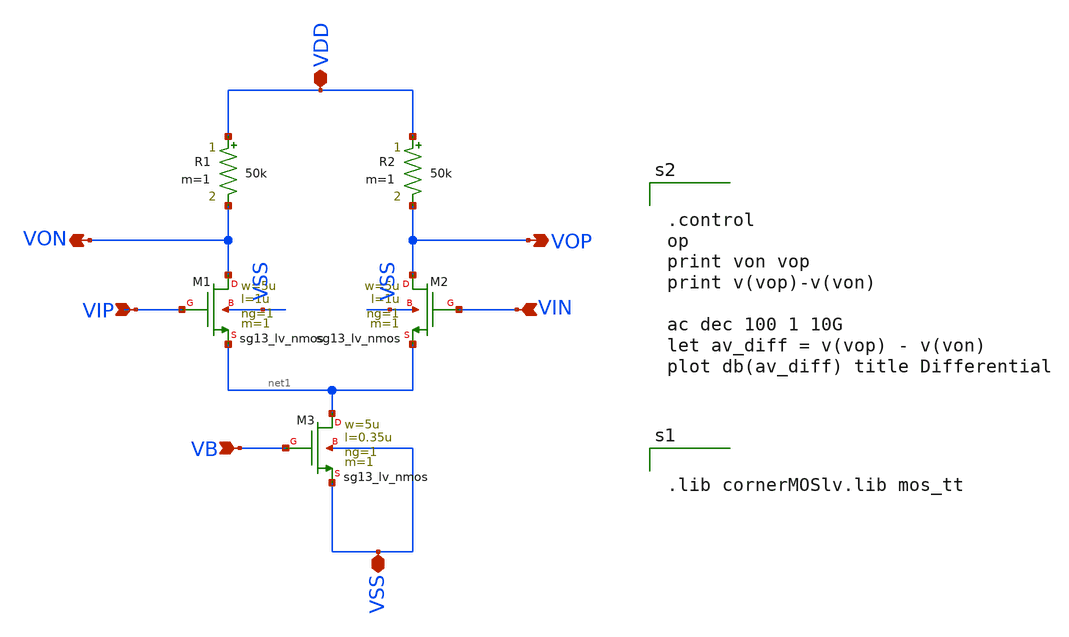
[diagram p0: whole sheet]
** sch_path: BTDay4-Ex/diff_pair_res.sch
**.subckt diff_pair_res VDD VSS VOP VON VIP VB VIN
*.iopin VDD
*.iopin VSS
*.opin VOP
*.opin VON
*.ipin VIP
*.ipin VB
*.ipin VIN
XM1 VON VIP net1 VSS sg13_lv_nmos w=5u l=1u ng=1 m=1 mm_ok=1
XM2 VOP VIN net1 VSS sg13_lv_nmos w=5u l=1u ng=1 m=1 mm_ok=1
XM3 net1 VB VSS VSS sg13_lv_nmos w=5u l=0.35u ng=1 m=1 mm_ok=1
R1 VDD VON 50k m=1
R2 VDD VOP 50k m=1
**** begin user architecture code


.lib cornerMOSlv.lib mos_tt




.control
op
print von vop
print v(vop)-v(von)

ac dec 100 1 10G
let av_diff = v(vop) - v(von)
plot db(av_diff) title Differential

**** end user architecture code
**.ends
.end
